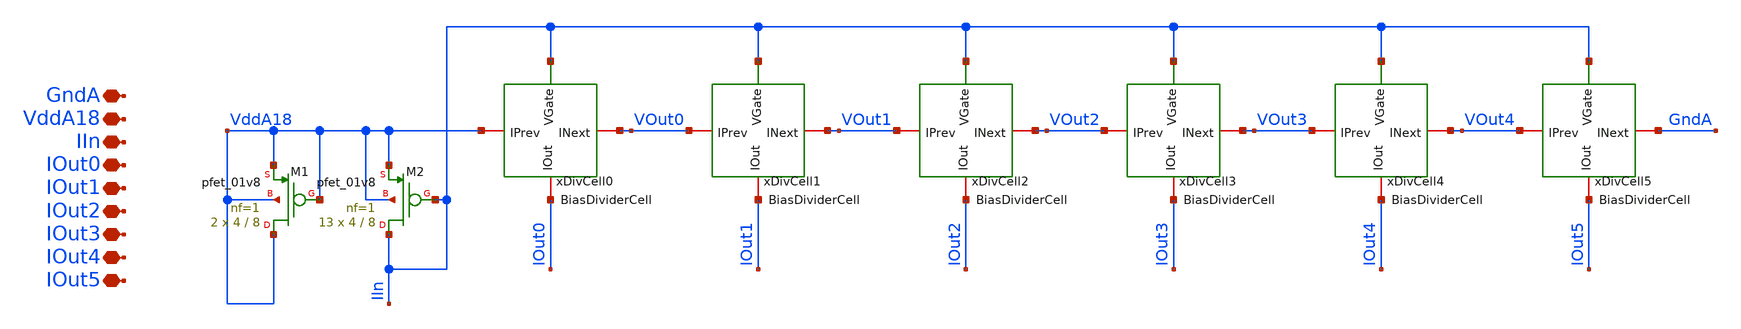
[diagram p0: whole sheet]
** sch_path: analog/klayout/production/final_merge_20260923/testbenches/cace/analog/xschem/BiasDivider_correct_no_cap.sch
**.subckt BiasDivider_correct_no_cap GndA VddA18 IIn IOut0 IOut1 IOut2 IOut3 IOut4 IOut5
*.iopin GndA
*.iopin VddA18
*.iopin IIn
*.iopin IOut0
*.iopin IOut1
*.iopin IOut2
*.iopin IOut3
*.iopin IOut4
*.iopin IOut5
xDivCell0 VddA18 VOut0 IIn IOut0 BiasDividerCell
XM1 VddA18 VddA18 VddA18 VddA18 sky130_fd_pr__pfet_01v8 L=8 W=4 nf=1 ad='int((1 + 1)/2) * 4 / 1 * 0.29'
+ as='int((1 + 2)/2) * 4 / 1 * 0.29' pd='2*int((1 + 1)/2) * (4 / 1 + 0.29)' ps='2*int((1 + 2)/2) * (4 / 1 + 0.29)'
+ nrd='0.29 / 4 ' nrs='0.29 / 4 ' sa=0 sb=0 sd=0 mult=2 m=2
XM2 IIn IIn VddA18 VddA18 sky130_fd_pr__pfet_01v8 L=8 W=4 nf=1 ad='int((1 + 1)/2) * 4 / 1 * 0.29' as='int((1 + 2)/2) * 4 / 1 * 0.29'
+ pd='2*int((1 + 1)/2) * (4 / 1 + 0.29)' ps='2*int((1 + 2)/2) * (4 / 1 + 0.29)' nrd='0.29 / 4 ' nrs='0.29 / 4 '
+ sa=0 sb=0 sd=0 mult=13 m=13
xDivCell5 VOut4 GndA IIn IOut5 BiasDividerCell
xDivCell1 VOut0 VOut1 IIn IOut1 BiasDividerCell
xDivCell2 VOut1 VOut2 IIn IOut2 BiasDividerCell
xDivCell3 VOut2 VOut3 IIn IOut3 BiasDividerCell
xDivCell4 VOut3 VOut4 IIn IOut4 BiasDividerCell
**.ends
.end
